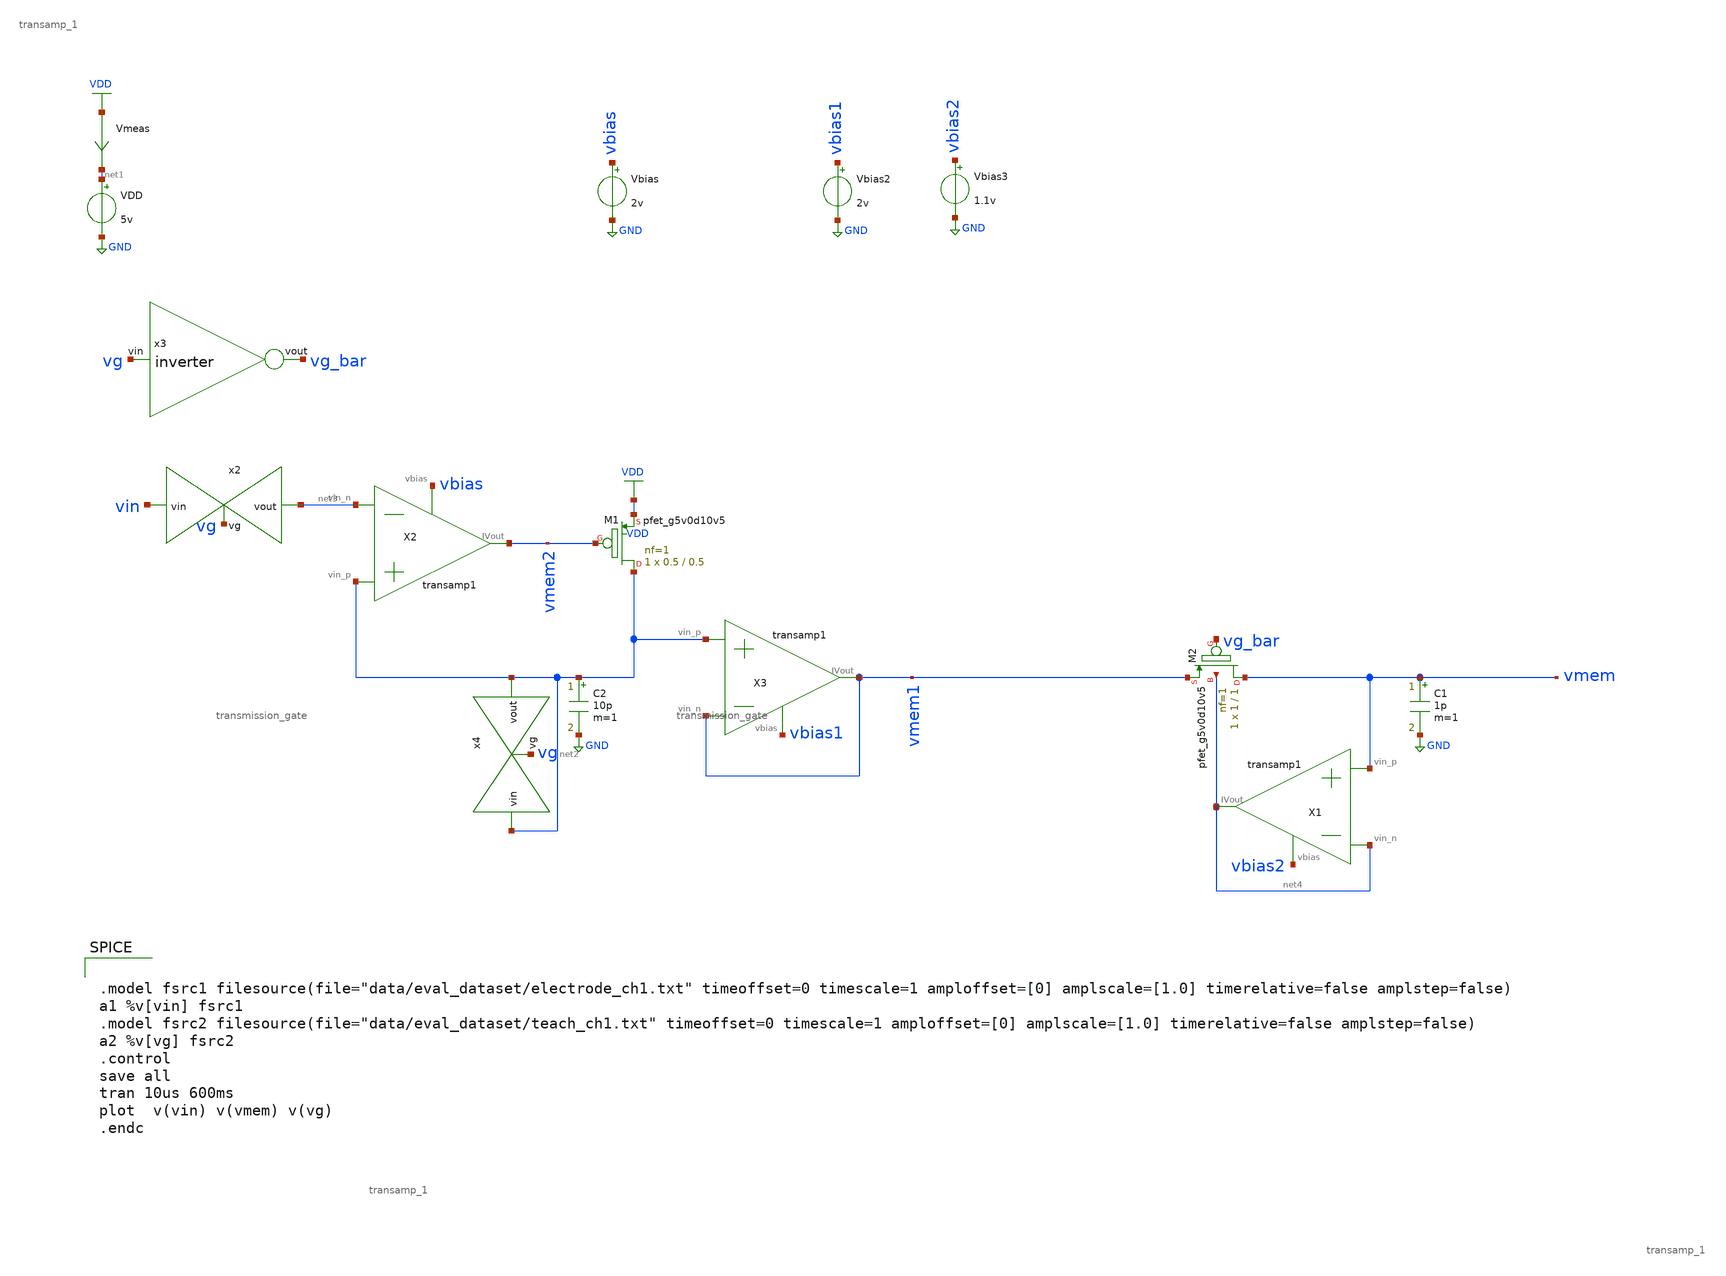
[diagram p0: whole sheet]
** sch_path: schematics/cap_mem_tb1.sch
**.subckt cap_mem_tb1
Vbias vbias GND 2v
VDD net1 GND 5v
Vmeas VDD net1 0
.save i(vmeas)
XM1 net2 vmem2 VDD VDD sky130_fd_pr__pfet_g5v0d10v5 L=0.5 W=0.5 nf=1 ad='int((nf+1)/2) * W/nf * 0.29'
+ as='int((nf+2)/2) * W/nf * 0.29' pd='2*int((nf+1)/2) * (W/nf + 0.29)' ps='2*int((nf+2)/2) * (W/nf + 0.29)'
+ nrd='0.29 / W' nrs='0.29 / W' sa=0 sb=0 sd=0 mult=1 m=1
C2 net2 GND 10p m=1
X2 net2 net3 vmem2 vbias transamp_1
x2 vin net3 vg transmission_gate
XM2 vmem vg_bar vmem1 net4 sky130_fd_pr__pfet_g5v0d10v5 L=1 W=1 nf=1 ad='int((nf+1)/2) * W/nf * 0.29'
+ as='int((nf+2)/2) * W/nf * 0.29' pd='2*int((nf+1)/2) * (W/nf + 0.29)' ps='2*int((nf+2)/2) * (W/nf + 0.29)'
+ nrd='0.29 / W' nrs='0.29 / W' sa=0 sb=0 sd=0 mult=1 m=1
X1 vmem net4 net4 vbias2 transamp_1
C1 vmem GND 1p m=1
X3 net2 vmem1 vmem1 vbias1 transamp_1
Vbias2 vbias1 GND 2v
Vbias3 vbias2 GND 1.1v
x3 vg_bar vg inverter
x4 net2 net2 vg transmission_gate
**** begin user architecture code


.model fsrc1 filesource(file="data/eval_dataset/electrode_ch1.txt" timeoffset=0 timescale=1
+ amploffset=[0] amplscale=[1.0] timerelative=false amplstep=false)
a1 %v[vin] fsrc1
.model fsrc2 filesource(file="data/eval_dataset/teach_ch1.txt" timeoffset=0 timescale=1
+ amploffset=[0] amplscale=[1.0] timerelative=false amplstep=false)
a2 %v[vg] fsrc2
.control
save all
tran 10us 600ms
plot  v(vin) v(vmem) v(vg)
.endc


 .lib $::SKYWATER_MODELS/models/sky130.lib.spice tt

.param mc_mm_switch=0
.param mc_pr_switch=1

**** end user architecture code
**.ends

* expanding   symbol:  /media/sf_share/final_project/transamp_1.sym # of pins=4
** sym_path: schematics/transamp_1.sym
** sch_path: schematics/transamp_1.sch
.subckt transamp_1 vin_p vin_n IVout vbias
*.opin IVout
*.ipin vin_p
*.ipin vin_n
*.ipin vbias
XM1 net1 vbias GND GND sky130_fd_pr__nfet_g5v0d10v5 L=1 W=1 nf=1 ad='int((nf+1)/2) * W/nf * 0.29' as='int((nf+2)/2) * W/nf * 0.29'
+ pd='2*int((nf+1)/2) * (W/nf + 0.29)' ps='2*int((nf+2)/2) * (W/nf + 0.29)' nrd='0.29 / W' nrs='0.29 / W'
+ sa=0 sb=0 sd=0 mult=1 m=1
XM3 net2 vin_p net1 GND sky130_fd_pr__nfet_g5v0d10v5 L=1 W=1 nf=1 ad='int((nf+1)/2) * W/nf * 0.29' as='int((nf+2)/2) * W/nf * 0.29'
+ pd='2*int((nf+1)/2) * (W/nf + 0.29)' ps='2*int((nf+2)/2) * (W/nf + 0.29)' nrd='0.29 / W' nrs='0.29 / W'
+ sa=0 sb=0 sd=0 mult=1 m=1
XM4 IVout net2 VDD VDD sky130_fd_pr__pfet_g5v0d10v5 L=1 W=1 nf=1 ad='int((nf+1)/2) * W/nf * 0.29' as='int((nf+2)/2) * W/nf * 0.29'
+ pd='2*int((nf+1)/2) * (W/nf + 0.29)' ps='2*int((nf+2)/2) * (W/nf + 0.29)' nrd='0.29 / W' nrs='0.29 / W'
+ sa=0 sb=0 sd=0 mult=1 m=1
XM2 IVout vin_n net1 GND sky130_fd_pr__nfet_g5v0d10v5 L=1 W=1 nf=1 ad='int((nf+1)/2) * W/nf * 0.29' as='int((nf+2)/2) * W/nf * 0.29'
+ pd='2*int((nf+1)/2) * (W/nf + 0.29)' ps='2*int((nf+2)/2) * (W/nf + 0.29)' nrd='0.29 / W' nrs='0.29 / W'
+ sa=0 sb=0 sd=0 mult=1 m=1
XM5 net2 net2 VDD VDD sky130_fd_pr__pfet_g5v0d10v5 L=1 W=1 nf=1 ad='int((nf+1)/2) * W/nf * 0.29' as='int((nf+2)/2) * W/nf * 0.29'
+ pd='2*int((nf+1)/2) * (W/nf + 0.29)' ps='2*int((nf+2)/2) * (W/nf + 0.29)' nrd='0.29 / W' nrs='0.29 / W'
+ sa=0 sb=0 sd=0 mult=1 m=1
.ends


* expanding   symbol:  /media/sf_share/final_project/transmission_gate.sym # of pins=3
** sym_path: schematics/transmission_gate.sym
** sch_path: schematics/transmission_gate.sch
.subckt transmission_gate vin vout vg
*.ipin vin
*.ipin vg
*.opin vout
x1 vg_bar vg inverter
XM5 vin vg vout GND sky130_fd_pr__nfet_g5v0d10v5 L=0.5 W=0.5 nf=1 ad='int((nf+1)/2) * W/nf * 0.29' as='int((nf+2)/2) * W/nf * 0.29'
+ pd='2*int((nf+1)/2) * (W/nf + 0.29)' ps='2*int((nf+2)/2) * (W/nf + 0.29)' nrd='0.29 / W' nrs='0.29 / W'
+ sa=0 sb=0 sd=0 mult=1 m=1
XM7 vout vg_bar vin VDD sky130_fd_pr__pfet_g5v0d10v5 L=0.5 W=0.5 nf=1 ad='int((nf+1)/2) * W/nf * 0.29'
+ as='int((nf+2)/2) * W/nf * 0.29' pd='2*int((nf+1)/2) * (W/nf + 0.29)' ps='2*int((nf+2)/2) * (W/nf + 0.29)'
+ nrd='0.29 / W' nrs='0.29 / W' sa=0 sb=0 sd=0 mult=1 m=1
XM6 vout vg_bar GND GND sky130_fd_pr__nfet_g5v0d10v5 L=0.5 W=0.5 nf=1 ad='int((nf+1)/2) * W/nf * 0.29'
+ as='int((nf+2)/2) * W/nf * 0.29' pd='2*int((nf+1)/2) * (W/nf + 0.29)' ps='2*int((nf+2)/2) * (W/nf + 0.29)'
+ nrd='0.29 / W' nrs='0.29 / W' sa=0 sb=0 sd=0 mult=1 m=1
.ends


* expanding   symbol:  /media/sf_share/final_project/inverter.sym # of pins=2
** sym_path: schematics/inverter.sym
** sch_path: schematics/inverter.sch
.subckt inverter vout vin
*.ipin vin
*.opin vout
XM3 vout vin VDD VDD sky130_fd_pr__pfet_g5v0d10v5 L=0.5 W=0.5 nf=1 ad='int((nf+1)/2) * W/nf * 0.29' as='int((nf+2)/2) * W/nf * 0.29'
+ pd='2*int((nf+1)/2) * (W/nf + 0.29)' ps='2*int((nf+2)/2) * (W/nf + 0.29)' nrd='0.29 / W' nrs='0.29 / W'
+ sa=0 sb=0 sd=0 mult=1 m=1
XM5 vout vin GND GND sky130_fd_pr__nfet_g5v0d10v5 L=0.5 W=0.5 nf=1 ad='int((nf+1)/2) * W/nf * 0.29' as='int((nf+2)/2) * W/nf * 0.29'
+ pd='2*int((nf+1)/2) * (W/nf + 0.29)' ps='2*int((nf+2)/2) * (W/nf + 0.29)' nrd='0.29 / W' nrs='0.29 / W'
+ sa=0 sb=0 sd=0 mult=1 m=1
.ends

.GLOBAL GND
.GLOBAL VDD
.end
